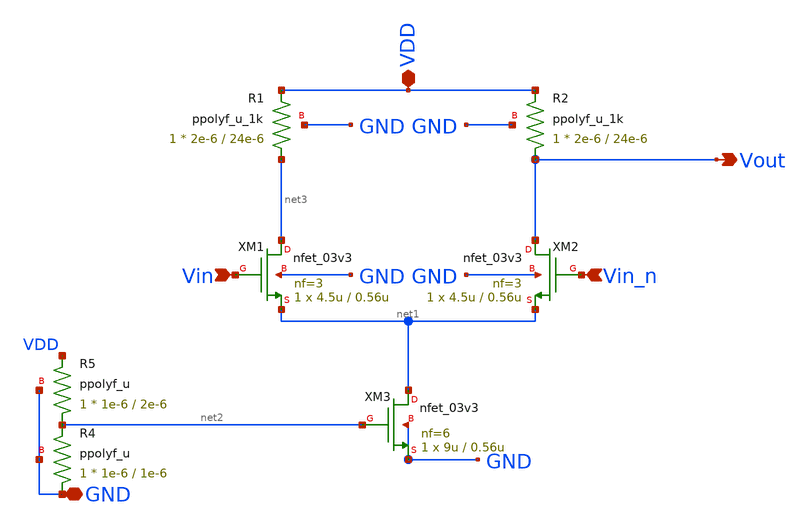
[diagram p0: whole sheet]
** sch_path: pll_block_templates_v1/layout2/diffpair.sch
**.subckt diffpair Vin Vin_n VDD Vout GND
*.ipin Vin
*.ipin Vin_n
*.iopin VDD
*.opin Vout
*.iopin GND
XM1 net3 Vin net1 GND nfet_03v3 L=0.56u W=4.5u nf=3 ad='int((nf+1)/2) * W/nf * 0.18u' as='int((nf+2)/2) * W/nf * 0.18u'
+ pd='2*int((nf+1)/2) * (W/nf + 0.18u)' ps='2*int((nf+2)/2) * (W/nf + 0.18u)' nrd='0.18u / W' nrs='0.18u / W'
+ sa=0 sb=0 sd=0 m=1
XM2 Vout Vin_n net1 GND nfet_03v3 L=0.56u W=4.5u nf=3 ad='int((nf+1)/2) * W/nf * 0.18u' as='int((nf+2)/2) * W/nf * 0.18u'
+ pd='2*int((nf+1)/2) * (W/nf + 0.18u)' ps='2*int((nf+2)/2) * (W/nf + 0.18u)' nrd='0.18u / W' nrs='0.18u / W'
+ sa=0 sb=0 sd=0 m=1
XM3 net1 net2 GND GND nfet_03v3 L=0.56u W=9u nf=6 ad='int((nf+1)/2) * W/nf * 0.18u' as='int((nf+2)/2) * W/nf * 0.18u'
+ pd='2*int((nf+1)/2) * (W/nf + 0.18u)' ps='2*int((nf+2)/2) * (W/nf + 0.18u)' nrd='0.18u / W' nrs='0.18u / W'
+ sa=0 sb=0 sd=0 m=1
XR1 net3 VDD GND ppolyf_u_1k r_width=2e-6 r_length=24e-6 m=1
XR2 Vout VDD GND ppolyf_u_1k r_width=2e-6 r_length=24e-6 m=1
XR4 GND net2 GND ppolyf_u r_width=1e-6 r_length=1e-6 m=1
XR5 net2 VDD GND ppolyf_u r_width=1e-6 r_length=2e-6 m=1
**.ends
.end
